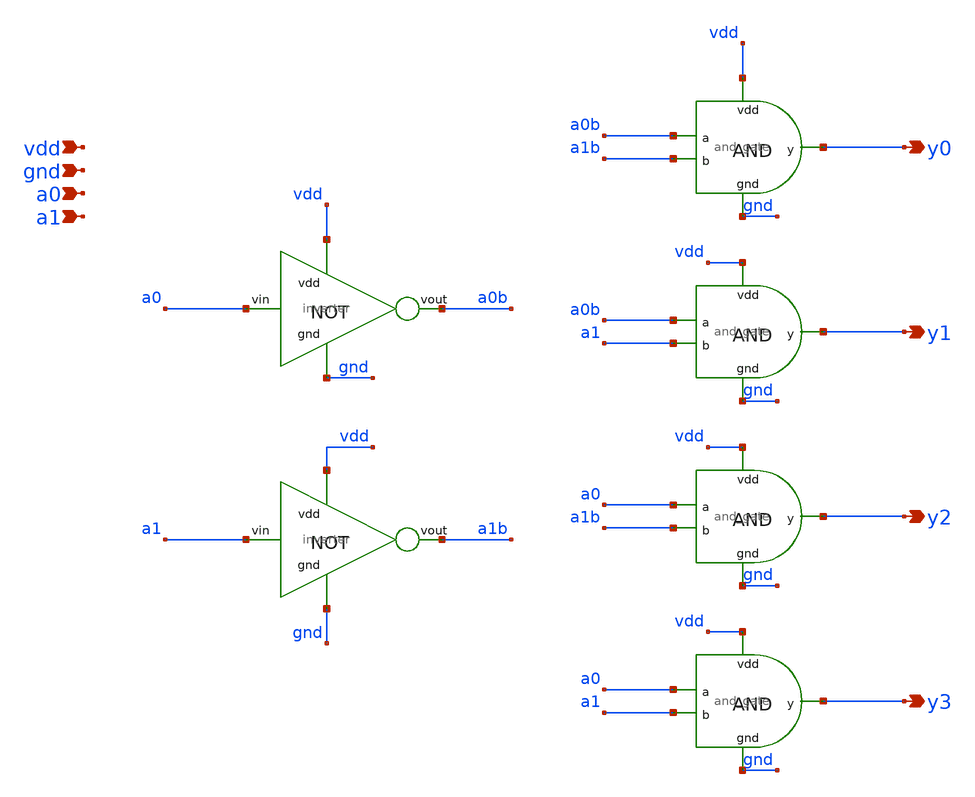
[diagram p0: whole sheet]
** sch_path: sram/decoder_2to4.sch
**.subckt decoder_2to4 y0 y1 y2 y3 vdd gnd a0 a1
*.opin y0
*.opin y1
*.opin y2
*.opin y3
*.ipin vdd
*.ipin gnd
*.ipin a0
*.ipin a1
x1 vdd a0b y0 a1b gnd and_gate
x2 vdd a0 a0b gnd inverter
x3 vdd a0b y1 a1 gnd and_gate
x4 vdd a0 y2 a1b gnd and_gate
x5 vdd a0 y3 a1 gnd and_gate
x6 vdd a1 a1b gnd inverter
**.ends

* expanding   symbol:  and_gate.sym # of pins=5
** sym_path: sram/and_gate.sym
** sch_path: sram/and_gate.sch
.subckt and_gate vdd a y b gnd
*.ipin a
*.ipin b
*.ipin vdd
*.ipin gnd
*.opin y
x2 vdd net1 y gnd inverter
x1 vdd a b gnd net1 nand_gate
.ends


* expanding   symbol:  inverter.sym # of pins=4
** sym_path: sram/inverter.sym
** sch_path: sram/inverter.sch
.subckt inverter vdd vin vout gnd
*.ipin vin
*.ipin vdd
*.ipin gnd
*.opin vout
XM1 vout vin gnd gnd sky130_fd_pr__nfet_01v8 L=0.15 W=1 nf=1 ad='int((nf+1)/2) * W/nf * 0.29' as='int((nf+2)/2) * W/nf * 0.29'
+ pd='2*int((nf+1)/2) * (W/nf + 0.29)' ps='2*int((nf+2)/2) * (W/nf + 0.29)' nrd='0.29 / W' nrs='0.29 / W'
+ sa=0 sb=0 sd=0 mult=1 m=1
XM2 vout vin vdd vdd sky130_fd_pr__pfet_01v8 L=0.15 W=1 nf=1 ad='int((nf+1)/2) * W/nf * 0.29' as='int((nf+2)/2) * W/nf * 0.29'
+ pd='2*int((nf+1)/2) * (W/nf + 0.29)' ps='2*int((nf+2)/2) * (W/nf + 0.29)' nrd='0.29 / W' nrs='0.29 / W'
+ sa=0 sb=0 sd=0 mult=1 m=1
.ends


* expanding   symbol:  nand_gate.sym # of pins=5
** sym_path: sram/nand_gate.sym
** sch_path: sram/nand_gate.sch
.subckt nand_gate vdd a b gnd y
*.ipin a
*.ipin b
*.ipin vdd
*.ipin gnd
*.opin y
XM1 y a vdd vdd sky130_fd_pr__pfet_01v8 L=0.15 W=1 nf=1 ad='int((nf+1)/2) * W/nf * 0.29' as='int((nf+2)/2) * W/nf * 0.29'
+ pd='2*int((nf+1)/2) * (W/nf + 0.29)' ps='2*int((nf+2)/2) * (W/nf + 0.29)' nrd='0.29 / W' nrs='0.29 / W'
+ sa=0 sb=0 sd=0 mult=1 m=1
XM2 y a net1 net1 sky130_fd_pr__nfet_01v8 L=0.15 W=1 nf=1 ad='int((nf+1)/2) * W/nf * 0.29' as='int((nf+2)/2) * W/nf * 0.29'
+ pd='2*int((nf+1)/2) * (W/nf + 0.29)' ps='2*int((nf+2)/2) * (W/nf + 0.29)' nrd='0.29 / W' nrs='0.29 / W'
+ sa=0 sb=0 sd=0 mult=1 m=1
XM3 y b vdd vdd sky130_fd_pr__pfet_01v8 L=0.15 W=1 nf=1 ad='int((nf+1)/2) * W/nf * 0.29' as='int((nf+2)/2) * W/nf * 0.29'
+ pd='2*int((nf+1)/2) * (W/nf + 0.29)' ps='2*int((nf+2)/2) * (W/nf + 0.29)' nrd='0.29 / W' nrs='0.29 / W'
+ sa=0 sb=0 sd=0 mult=1 m=1
XM4 net1 b gnd gnd sky130_fd_pr__nfet_01v8 L=0.15 W=1 nf=1 ad='int((nf+1)/2) * W/nf * 0.29' as='int((nf+2)/2) * W/nf * 0.29'
+ pd='2*int((nf+1)/2) * (W/nf + 0.29)' ps='2*int((nf+2)/2) * (W/nf + 0.29)' nrd='0.29 / W' nrs='0.29 / W'
+ sa=0 sb=0 sd=0 mult=1 m=1
.ends

.end
